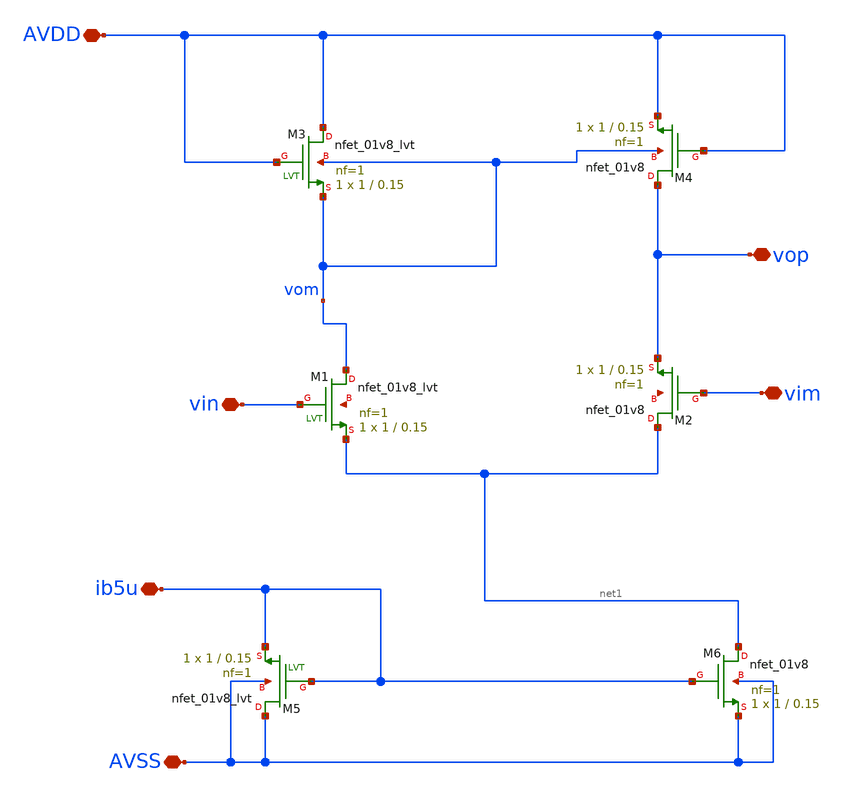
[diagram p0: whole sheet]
** sch_path: xschem/data.sch
**.subckt data vop ib5u vin vim AVSS AVDD
*.iopin vop
*.iopin ib5u
*.iopin vin
*.iopin vim
*.iopin AVSS
*.iopin AVDD
XM1 vom vin net1 net2 sky130_fd_pr__nfet_01v8_lvt L=0.15 W=1 nf=1 ad='int((1 + 1)/2) * 1 / 1 * 0.29'
+ as='int((1 + 2)/2) * 1 / 1 * 0.29' pd='2*int((1 + 1)/2) * (1 / 1 + 0.29)' ps='2*int((1 + 2)/2) * (1 / 1 + 0.29)'
+ nrd='0.29 / 1 ' nrs='0.29 / 1 ' sa=0 sb=0 sd=0 mult=1 m=1
XM2 net1 vim vop net3 sky130_fd_pr__nfet_01v8 L=0.15 W=1 nf=1 ad='int((1 + 1)/2) * 1 / 1 * 0.29' as='int((1 + 2)/2) * 1 / 1 * 0.29'
+ pd='2*int((1 + 1)/2) * (1 / 1 + 0.29)' ps='2*int((1 + 2)/2) * (1 / 1 + 0.29)' nrd='0.29 / 1 ' nrs='0.29 / 1 '
+ sa=0 sb=0 sd=0 mult=1 m=1
XM3 AVDD AVDD vom vom sky130_fd_pr__nfet_01v8_lvt L=0.15 W=1 nf=1 ad='int((1 + 1)/2) * 1 / 1 * 0.29'
+ as='int((1 + 2)/2) * 1 / 1 * 0.29' pd='2*int((1 + 1)/2) * (1 / 1 + 0.29)' ps='2*int((1 + 2)/2) * (1 / 1 + 0.29)'
+ nrd='0.29 / 1 ' nrs='0.29 / 1 ' sa=0 sb=0 sd=0 mult=1 m=1
XM4 vop AVDD AVDD vom sky130_fd_pr__nfet_01v8 L=0.15 W=1 nf=1 ad='int((1 + 1)/2) * 1 / 1 * 0.29' as='int((1 + 2)/2) * 1 / 1 * 0.29'
+ pd='2*int((1 + 1)/2) * (1 / 1 + 0.29)' ps='2*int((1 + 2)/2) * (1 / 1 + 0.29)' nrd='0.29 / 1 ' nrs='0.29 / 1 '
+ sa=0 sb=0 sd=0 mult=1 m=1
XM5 AVSS ib5u ib5u AVSS sky130_fd_pr__nfet_01v8_lvt L=0.15 W=1 nf=1 ad='int((1 + 1)/2) * 1 / 1 * 0.29'
+ as='int((1 + 2)/2) * 1 / 1 * 0.29' pd='2*int((1 + 1)/2) * (1 / 1 + 0.29)' ps='2*int((1 + 2)/2) * (1 / 1 + 0.29)'
+ nrd='0.29 / 1 ' nrs='0.29 / 1 ' sa=0 sb=0 sd=0 mult=1 m=1
XM6 net1 ib5u AVSS AVSS sky130_fd_pr__nfet_01v8 L=0.15 W=1 nf=1 ad='int((1 + 1)/2) * 1 / 1 * 0.29' as='int((1 + 2)/2) * 1 / 1 * 0.29'
+ pd='2*int((1 + 1)/2) * (1 / 1 + 0.29)' ps='2*int((1 + 2)/2) * (1 / 1 + 0.29)' nrd='0.29 / 1 ' nrs='0.29 / 1 '
+ sa=0 sb=0 sd=0 mult=1 m=1
**.ends
.end
